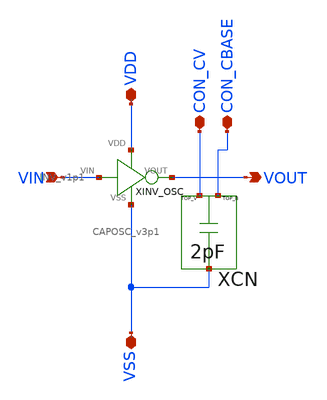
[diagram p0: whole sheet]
** sch_path: samples/cace-tests/SDC/xschem/INVandCAP_v4p1.sch
**.subckt INVandCAP_v4p1 VIN VDD VSS VOUT CON_CV CON_CBASE
*.ipin VIN
*.iopin VDD
*.iopin VSS
*.opin VOUT
*.iopin CON_CV
*.iopin CON_CBASE
XINV_OSC VIN VOUT VDD VSS INV_v1p1
XCN CON_CV CON_CBASE VSS CAPOSC_v3p1
**.ends

* expanding   symbol:  INV_v1p1.sym # of pins=4
** sym_path: samples/cace-tests/SDC/xschem/INV_v1p1.sym
** sch_path: samples/cace-tests/SDC/xschem/INV_v1p1.sch
.subckt INV_v1p1 VIN VOUT VDD VSS
*.ipin VIN
*.iopin VDD
*.iopin VSS
*.opin VOUT
XM1 VOUT VIN VSS VSS sky130_fd_pr__nfet_01v8 L=0.15 W=2 nf=2 ad='int((nf+1)/2) * W/nf * 0.29' as='int((nf+2)/2) * W/nf * 0.29'
+ pd='2*int((nf+1)/2) * (W/nf + 0.29)' ps='2*int((nf+2)/2) * (W/nf + 0.29)' nrd='0.29 / W' nrs='0.29 / W'
+ sa=0 sb=0 sd=0 mult=1 m=1
XM2 VOUT VIN VDD VDD sky130_fd_pr__pfet_01v8 L=0.15 W=6 nf=6 ad='int((nf+1)/2) * W/nf * 0.29' as='int((nf+2)/2) * W/nf * 0.29'
+ pd='2*int((nf+1)/2) * (W/nf + 0.29)' ps='2*int((nf+2)/2) * (W/nf + 0.29)' nrd='0.29 / W' nrs='0.29 / W'
+ sa=0 sb=0 sd=0 mult=1 m=1
.ends


* expanding   symbol:  CAPOSC_v3p1.sym # of pins=3
** sym_path: samples/cace-tests/SDC/xschem/CAPOSC_v3p1.sym
** sch_path: samples/cace-tests/SDC/xschem/CAPOSC_v3p1.sch
.subckt CAPOSC_v3p1 TOP_V TOP_B BOT
*.iopin TOP_V
*.iopin TOP_B
*.iopin BOT
XC1_V TOP_V BOT sky130_fd_pr__cap_mim_m3_1 W=10 L=10 MF=1 m=1
XC2_V TOP_V BOT sky130_fd_pr__cap_mim_m3_2 W=10 L=10 MF=1 m=1
XC1_B TOP_B BOT sky130_fd_pr__cap_mim_m3_1 W=10 L=10 MF=1 m=1
XC2_B TOP_B BOT sky130_fd_pr__cap_mim_m3_2 W=10 L=10 MF=1 m=1
XC5_B TOP_B BOT sky130_fd_pr__cap_mim_m3_1 W=10 L=10 MF=1 m=1
XC6_B TOP_B BOT sky130_fd_pr__cap_mim_m3_2 W=10 L=10 MF=1 m=1
XC3_B TOP_B BOT sky130_fd_pr__cap_mim_m3_1 W=10 L=10 MF=1 m=1
XC4_B TOP_B BOT sky130_fd_pr__cap_mim_m3_2 W=10 L=10 MF=1 m=1
XC7_B TOP_B BOT sky130_fd_pr__cap_mim_m3_1 W=10 L=10 MF=1 m=1
XC8_B TOP_B BOT sky130_fd_pr__cap_mim_m3_2 W=10 L=10 MF=1 m=1
XC9_B TOP_B BOT sky130_fd_pr__cap_mim_m3_1 W=10 L=10 MF=1 m=1
XC10_B TOP_B BOT sky130_fd_pr__cap_mim_m3_2 W=10 L=10 MF=1 m=1
.ends

.end
